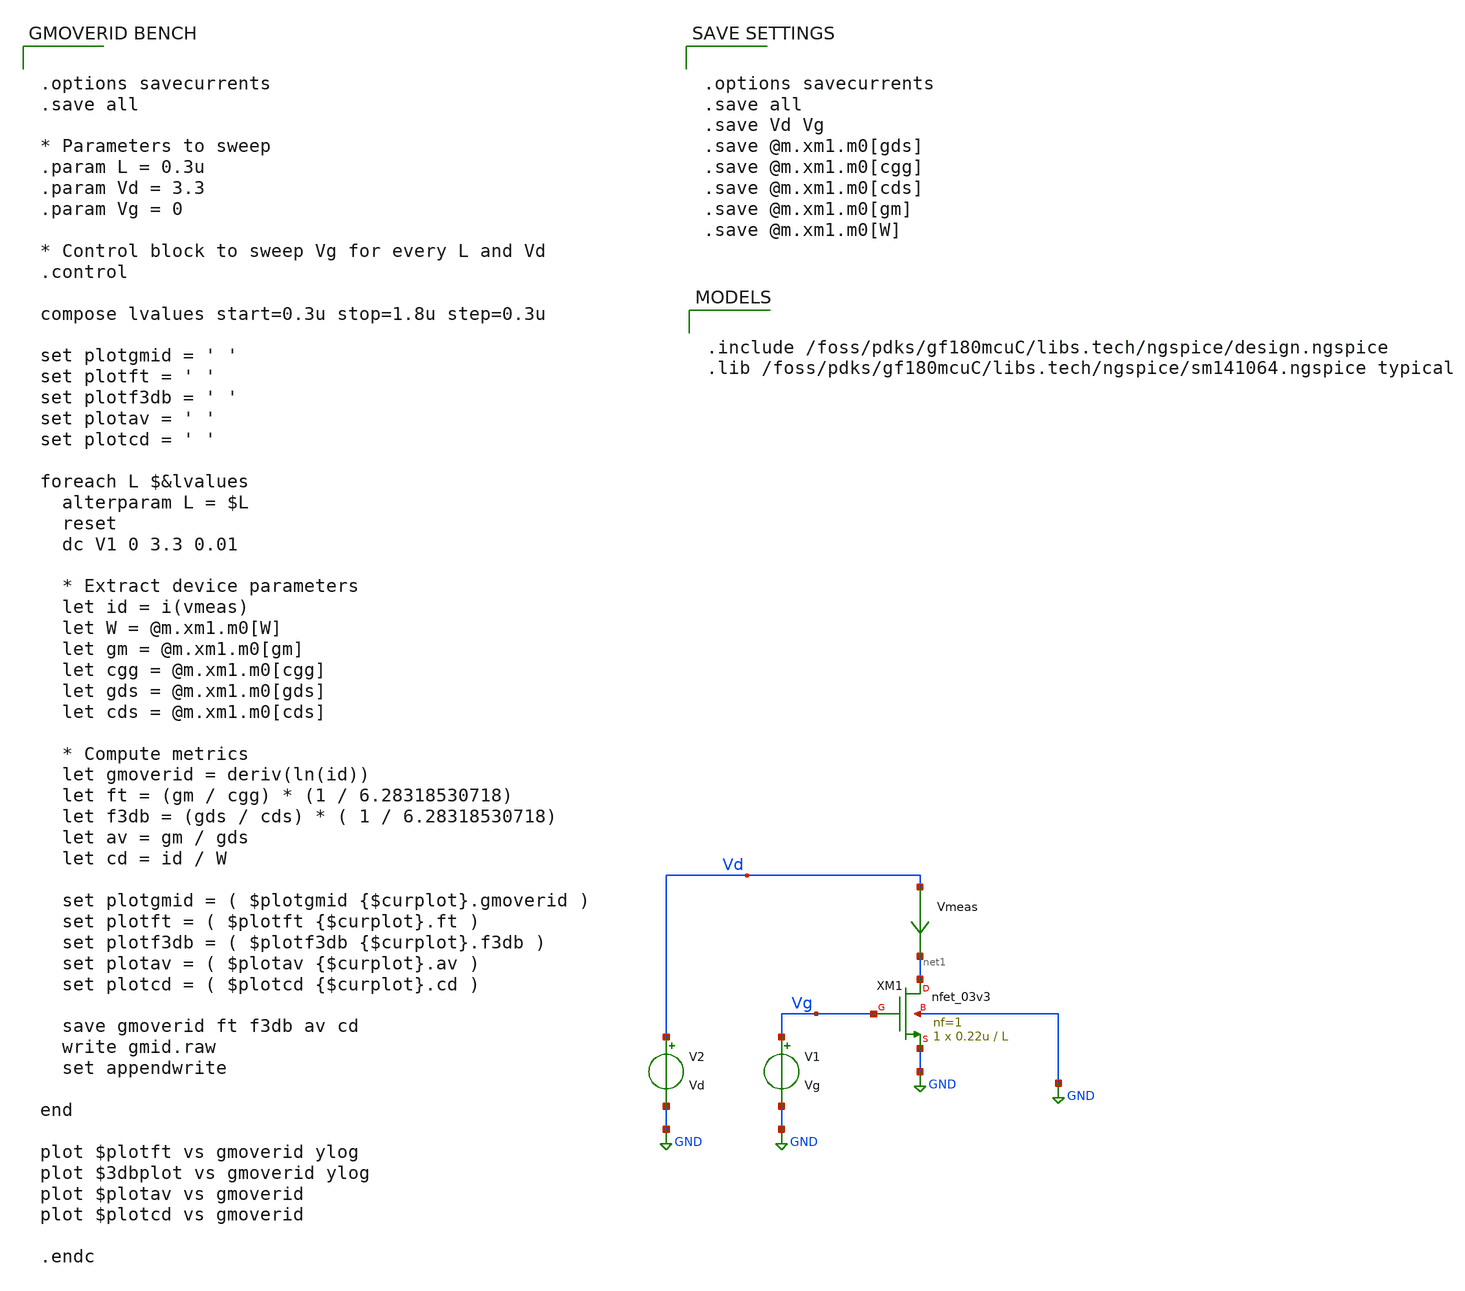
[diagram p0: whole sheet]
** sch_path: gf180mcuC/nfet_03v3_gmid.sch
**.subckt nfet_03v3_gmid
XM1 net1 Vg GND GND nfet_03v3 L=L W=0.22u nf=1 ad='int((nf+1)/2) * W/nf * 0.18u' as='int((nf+2)/2) * W/nf * 0.18u'
+ pd='2*int((nf+1)/2) * (W/nf + 0.18u)' ps='2*int((nf+2)/2) * (W/nf + 0.18u)' nrd='0.18u / W' nrs='0.18u / W'
+ sa=0 sb=0 sd=0 m=1
V1 Vg GND Vg
V2 Vd GND Vd
Vmeas Vd net1 0
.save i(vmeas)
**** begin user architecture code


.options savecurrents
.save all

* Parameters to sweep
.param L = 0.3u
.param Vd = 3.3
.param Vg = 0

* Control block to sweep Vg for every L and Vd
.control

compose lvalues start=0.3u stop=1.8u step=0.3u

set plotgmid = ' '
set plotft = ' '
set plotf3db = ' '
set plotav = ' '
set plotcd = ' '

foreach L $&lvalues
  alterparam L = $L
  reset
  dc V1 0 3.3 0.01

  * Extract device parameters
  let id = i(vmeas)
  let W = @m.xm1.m0[W]
  let gm = @m.xm1.m0[gm]
  let cgg = @m.xm1.m0[cgg]
  let gds = @m.xm1.m0[gds]
  let cds = @m.xm1.m0[cds]

  * Compute metrics
  let gmoverid = deriv(ln(id))
  let ft = (gm / cgg) * (1 / 6.28318530718)
  let f3db = (gds / cds) * ( 1 / 6.28318530718)
  let av = gm / gds
  let cd = id / W

  set plotgmid = ( $plotgmid {$curplot}.gmoverid )
  set plotft = ( $plotft {$curplot}.ft )
  set plotf3db = ( $plotf3db {$curplot}.f3db )
  set plotav = ( $plotav {$curplot}.av )
  set plotcd = ( $plotcd {$curplot}.cd )

  save gmoverid ft f3db av cd
  write gmid.raw
  set appendwrite

end

plot $plotft vs gmoverid ylog
plot $3dbplot vs gmoverid ylog
plot $plotav vs gmoverid
plot $plotcd vs gmoverid

.endc




.options savecurrents
.save all
.save Vd Vg
.save @m.xm1.m0[gds]
.save @m.xm1.m0[cgg]
.save @m.xm1.m0[cds]
.save @m.xm1.m0[gm]
.save @m.xm1.m0[W]



.include /foss/pdks/gf180mcuC/libs.tech/ngspice/design.ngspice
.lib /foss/pdks/gf180mcuC/libs.tech/ngspice/sm141064.ngspice typical

**** end user architecture code
**.ends
.GLOBAL GND
.end
